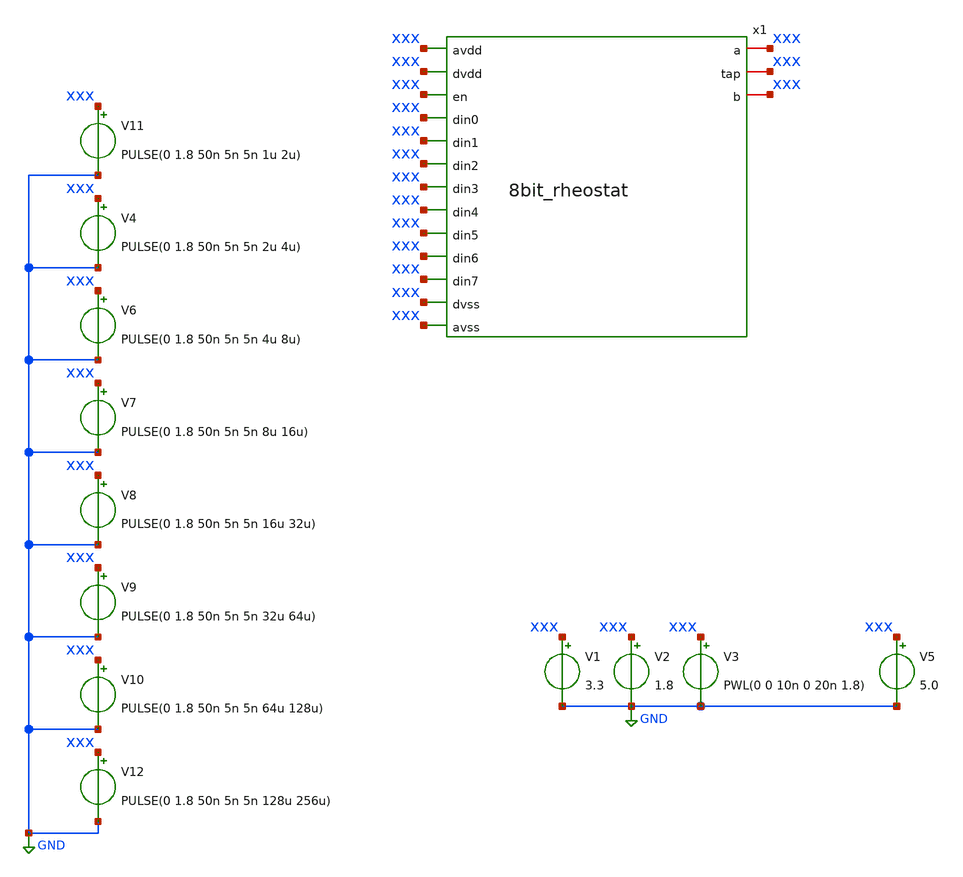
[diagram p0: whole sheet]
** sch_path: xschem/8bit_rheostat_tb.sch
**.subckt 8bit_rheostat_tb
x1 xxx xxx xxx xxx xxx xxx xxx xxx xxx xxx xxx xxx xxx xxx xxx xxx 8bit_rheostat
V11 xxx GND PULSE(0 1.8 50n 5n 5n 1u 2u)
V4 xxx GND PULSE(0 1.8 50n 5n 5n 2u 4u)
V6 xxx GND PULSE(0 1.8 50n 5n 5n 4u 8u)
V7 xxx GND PULSE(0 1.8 50n 5n 5n 8u 16u)
V8 xxx GND PULSE(0 1.8 50n 5n 5n 16u 32u)
V9 xxx GND PULSE(0 1.8 50n 5n 5n 32u 64u)
V10 xxx GND PULSE(0 1.8 50n 5n 5n 64u 128u)
V12 xxx GND PULSE(0 1.8 50n 5n 5n 128u 256u)
V1 xxx GND 3.3
V2 xxx GND 1.8
V3 xxx GND PWL(0 0 10n 0 20n 1.8)
V5 xxx GND 5.0
**** begin user architecture code


.lib /usr/share/pdk/sky130A/libs.tech/ngspice/sky130.lib.spice tt
.include /usr/share/pdk/sky130A/libs.ref/sky130_fd_sc_hvl/spice/sky130_fd_sc_hvl.spice




.control
tran 50m 256u
plot V(out)
.endc

**** end user architecture code
**.ends
.GLOBAL GND
.end
